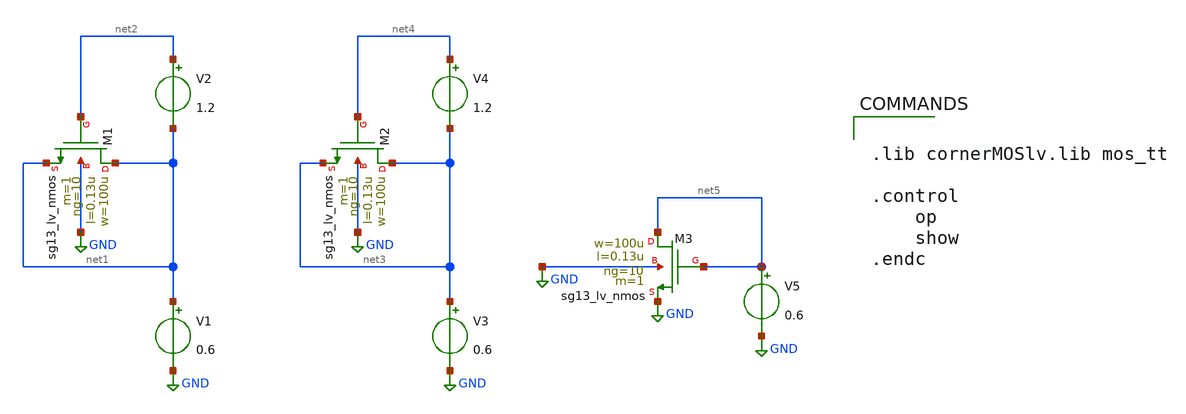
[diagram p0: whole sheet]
** sch_path: xschem/tb_op.sch
**.subckt tb_op
V1 net1 GND 0.6
V2 net2 net1 1.2
XM1 net1 net2 net1 GND sg13_lv_nmos w=100u l=0.13u ng=10 m=1 mm_ok=1
V3 net3 GND 0.6
V4 net4 net3 1.2
XM2 net3 net4 net3 GND sg13_lv_nmos w=100u l=0.13u ng=10 m=1 mm_ok=1
XM3 net5 net5 GND GND sg13_lv_nmos w=100u l=0.13u ng=10 m=1 mm_ok=1
V5 net5 GND 0.6
**** begin user architecture code


.lib cornerMOSlv.lib mos_tt

.control
    op
    show
.endc


**** end user architecture code
**.ends
.GLOBAL GND
.end
